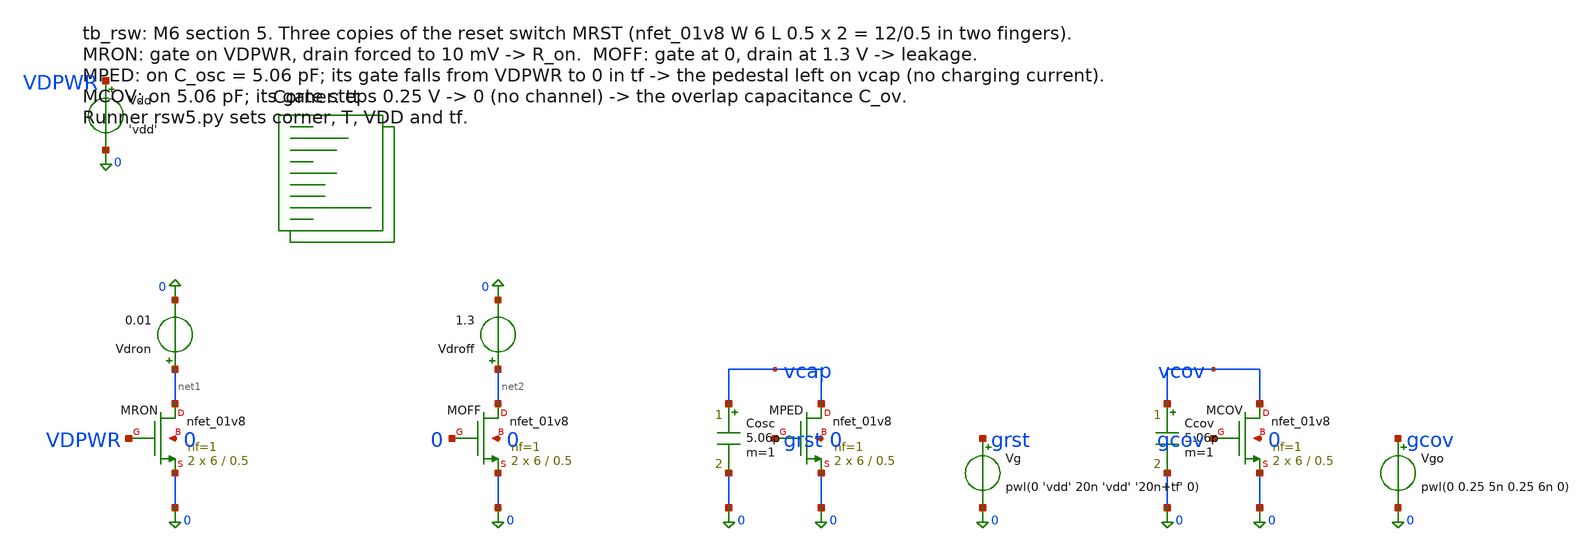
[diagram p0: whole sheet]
** sch_path: xschem/tb_rsw.sch
**.subckt tb_rsw
XMRON net1 VDPWR 0 0 sky130_fd_pr__nfet_01v8 L=0.5 W=6 nf=1 ad='int((1 + 1)/2) * 6 / 1 * 0.29' as='int((1 + 2)/2) * 6 / 1 * 0.29'
+ pd='2*int((1 + 1)/2) * (6 / 1 + 0.29)' ps='2*int((1 + 2)/2) * (6 / 1 + 0.29)' nrd='0.29 / 6 ' nrs='0.29 / 6 '
+ sa=0 sb=0 sd=0 mult=2 m=2
XMOFF net2 0 0 0 sky130_fd_pr__nfet_01v8 L=0.5 W=6 nf=1 ad='int((1 + 1)/2) * 6 / 1 * 0.29' as='int((1 + 2)/2) * 6 / 1 * 0.29'
+ pd='2*int((1 + 1)/2) * (6 / 1 + 0.29)' ps='2*int((1 + 2)/2) * (6 / 1 + 0.29)' nrd='0.29 / 6 ' nrs='0.29 / 6 '
+ sa=0 sb=0 sd=0 mult=2 m=2
XMPED vcap grst 0 0 sky130_fd_pr__nfet_01v8 L=0.5 W=6 nf=1 ad='int((1 + 1)/2) * 6 / 1 * 0.29' as='int((1 + 2)/2) * 6 / 1 * 0.29'
+ pd='2*int((1 + 1)/2) * (6 / 1 + 0.29)' ps='2*int((1 + 2)/2) * (6 / 1 + 0.29)' nrd='0.29 / 6 ' nrs='0.29 / 6 '
+ sa=0 sb=0 sd=0 mult=2 m=2
XMCOV vcov gcov 0 0 sky130_fd_pr__nfet_01v8 L=0.5 W=6 nf=1 ad='int((1 + 1)/2) * 6 / 1 * 0.29' as='int((1 + 2)/2) * 6 / 1 * 0.29'
+ pd='2*int((1 + 1)/2) * (6 / 1 + 0.29)' ps='2*int((1 + 2)/2) * (6 / 1 + 0.29)' nrd='0.29 / 6 ' nrs='0.29 / 6 '
+ sa=0 sb=0 sd=0 mult=2 m=2
Ccov vcov 0 5.06p m=1
Vgo gcov 0 pwl(0 0.25 5n 0.25 6n 0)
Cosc vcap 0 5.06p m=1
Vdron net1 0 0.01
Vdroff net2 0 1.3
Vg grst 0 pwl(0 'vdd' 20n 'vdd' '20n+tf' 0)
Vdd VDPWR 0 'vdd'
**** begin user architecture code
.lib $::SKYWATER_MODELS/sky130.lib.spice tt

.param vdd=1.8 tf=2n
.temp 25
.option method=gear
.control
op
let ron = 0.01/abs(i(vdron))
let ioff = abs(i(vdroff))*1e9
let cggon = @m.xmped.msky130_fd_pr__nfet_01v8[cgg]*1e15
let vth = @m.xmped.msky130_fd_pr__nfet_01v8[vth]
echo OP ron=$&ron ioff_nA=$&ioff cgg_on_fF=$&cggon vth=$&vth
tran 0.01n 72n 0 0.01n
* overlap only: MCOV's gate falls 0.25 V -> 0, far below threshold (no channel; a 0.5 V step already catches some
* weak-inversion charge); C_ov = -step * 5.06 pF / 0.25 V
meas tran cov find v(vcov) at=18n
let cov_fF = -cov*5.06e-12/0.25*1e15
meas tran ped find v(vcap) at=62n
let ped_mV = ped*1e3
echo PED ped_mV=$&ped_mV cov_fF=$&cov_fF
.endc

**** end user architecture code
**.ends
.end
